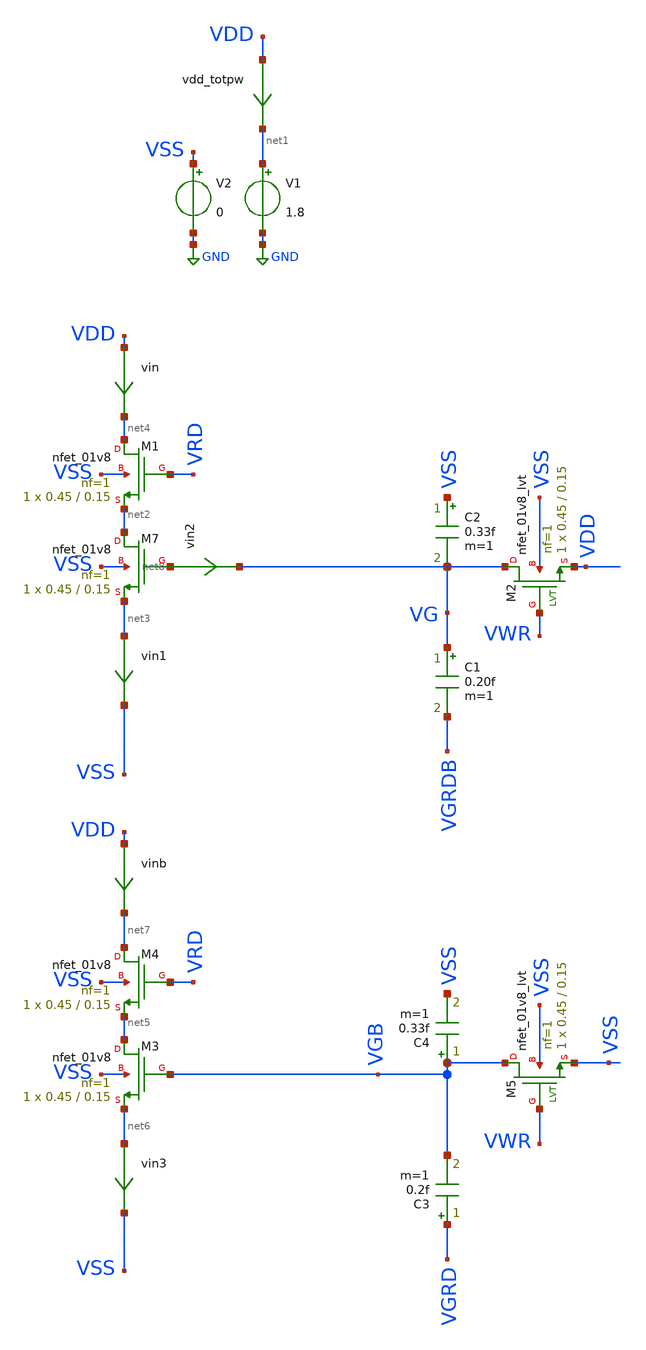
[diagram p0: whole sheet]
** sch_path: xschem/tb_dram3t_cap_interference.sch
**.subckt tb_dram3t_cap_interference
V1 net1 GND 1.8
V2 VSS GND 0
vdd_totpw VDD net1 0
.save i(vdd_totpw)
vin VDD net4 0
.save i(vin)
XM2 VG VWR VDD VSS sky130_fd_pr__nfet_01v8_lvt L=0.15 W=0.45 nf=1 ad='int((nf+1)/2) * W/nf * 0.29' as='int((nf+2)/2) * W/nf * 0.29'
+ pd='2*int((nf+1)/2) * (W/nf + 0.29)' ps='2*int((nf+2)/2) * (W/nf + 0.29)' nrd='0.29 / W' nrs='0.29 / W'
+ sa=0 sb=0 sd=0 mult=1 m=1
C1 VG VGRDB 0.20f m=1
C2 VSS VG 0.33f m=1
vin1 net3 VSS 0
.save i(vin1)
vin2 net8 VG 0
.save i(vin2)
vinb VDD net7 0
.save i(vinb)
XM5 VGB VWR VSS VSS sky130_fd_pr__nfet_01v8_lvt L=0.15 W=0.45 nf=1 ad='int((nf+1)/2) * W/nf * 0.29' as='int((nf+2)/2) * W/nf * 0.29'
+ pd='2*int((nf+1)/2) * (W/nf + 0.29)' ps='2*int((nf+2)/2) * (W/nf + 0.29)' nrd='0.29 / W' nrs='0.29 / W'
+ sa=0 sb=0 sd=0 mult=1 m=1
C3 VGRD VGB 0.2f m=1
C4 VGB VSS 0.33f m=1
XM7 net2 net8 net3 VSS sky130_fd_pr__nfet_01v8 L=0.15 W=0.45 nf=1 ad='int((nf+1)/2) * W/nf * 0.29' as='int((nf+2)/2) * W/nf * 0.29'
+ pd='2*int((nf+1)/2) * (W/nf + 0.29)' ps='2*int((nf+2)/2) * (W/nf + 0.29)' nrd='0.29 / W' nrs='0.29 / W'
+ sa=0 sb=0 sd=0 mult=1 m=1
XM1 net4 VRD net2 VSS sky130_fd_pr__nfet_01v8 L=0.15 W=0.45 nf=1 ad='int((nf+1)/2) * W/nf * 0.29' as='int((nf+2)/2) * W/nf * 0.29'
+ pd='2*int((nf+1)/2) * (W/nf + 0.29)' ps='2*int((nf+2)/2) * (W/nf + 0.29)' nrd='0.29 / W' nrs='0.29 / W'
+ sa=0 sb=0 sd=0 mult=1 m=1
vin3 net6 VSS 0
.save i(vin3)
XM3 net5 VGB net6 VSS sky130_fd_pr__nfet_01v8 L=0.15 W=0.45 nf=1 ad='int((nf+1)/2) * W/nf * 0.29' as='int((nf+2)/2) * W/nf * 0.29'
+ pd='2*int((nf+1)/2) * (W/nf + 0.29)' ps='2*int((nf+2)/2) * (W/nf + 0.29)' nrd='0.29 / W' nrs='0.29 / W'
+ sa=0 sb=0 sd=0 mult=1 m=1
XM4 net7 VRD net5 VSS sky130_fd_pr__nfet_01v8 L=0.15 W=0.45 nf=1 ad='int((nf+1)/2) * W/nf * 0.29' as='int((nf+2)/2) * W/nf * 0.29'
+ pd='2*int((nf+1)/2) * (W/nf + 0.29)' ps='2*int((nf+2)/2) * (W/nf + 0.29)' nrd='0.29 / W' nrs='0.29 / W'
+ sa=0 sb=0 sd=0 mult=1 m=1
**** begin user architecture code

** opencircuitdesign pdks install
.lib $::SKYWATER_MODELS/sky130.lib.spice tt_mm
*.lib $::SKYWATER_STDCELLS/sky130_fd_sc_hd_blablabla.spice

.subckt sky130_fd_sc_hd__inv_1 A VGND VNB VPB VPWR Y
X0 VGND A Y VNB sky130_fd_pr__nfet_01v8 w=650000u l=150000u
X1 VPWR A Y VPB sky130_fd_pr__pfet_01v8_hvt w=1e+06u l=150000u
.ends




* ngspice commands

.options savecurrents

VWR VWR     0 pulse 0 1.8  4n 0.2n 0.2n 2n 200n
VRD VRD     0 pulse 0 1.8 10n 0.2n 0.2n 2n 10n
VGRD VGRD   0 pulse 0 1.2 25n 0.2n 0.2n 2n 4n
VGRDB VGRDB 0 pulse 1.2 0 25n 0.2n 0.2n 2n 4n

.control
  repeat 20
    save all
    tran 0.05n 60n
    remzerovec
    write tb_dram3t_cap_interference.raw
    set appendwrite
    reset
    end
.endc




**** end user architecture code
**.ends
.GLOBAL GND
.end
